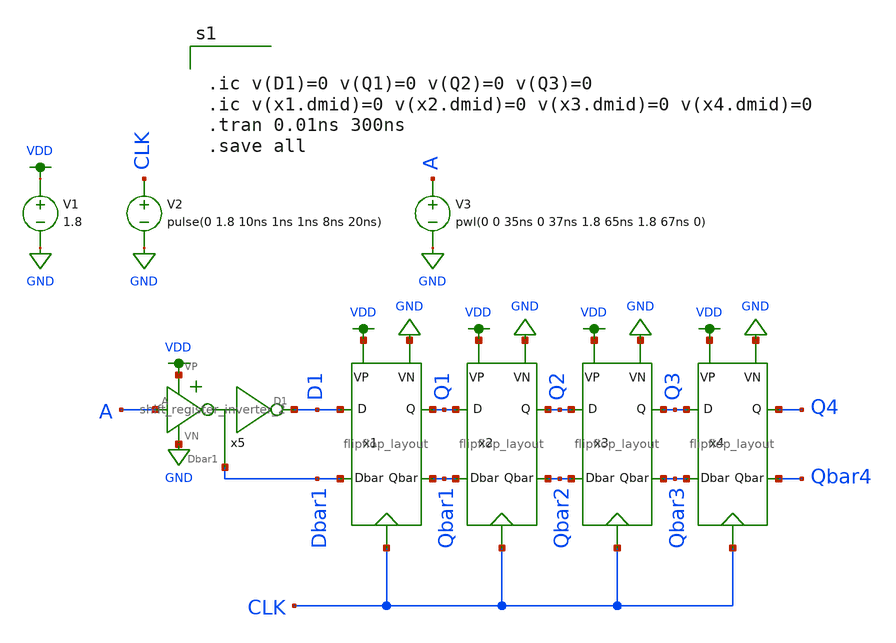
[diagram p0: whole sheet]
** sch_path: mp2/submission/Xschem/shift_register_test_sf.sch
**.subckt shift_register_test_sf
V1 VDD GND 1.8
V2 CLK GND pulse(0 1.8 10ns 1ns 1ns 8ns 20ns)
V3 A GND pwl(0 0 35ns 0 37ns 1.8 65ns 1.8 67ns 0)
x1 D1 VDD Dbar1 GND Q1 CLK Qbar1 flipflop_layout
x2 Q1 VDD Qbar1 GND Q2 CLK Qbar2 flipflop_layout
x3 Q2 VDD Qbar2 GND Q3 CLK Qbar3 flipflop_layout
x4 Q3 VDD Qbar3 GND Q4 CLK Qbar4 flipflop_layout
x5 VDD A D1 Dbar1 GND shift_register_inverter_2
**** begin user architecture code


.ic v(D1)=0 v(Q1)=0 v(Q2)=0 v(Q3)=0
.ic v(x1.dmid)=0 v(x2.dmid)=0 v(x3.dmid)=0 v(x4.dmid)=0
.tran 0.01ns 300ns
.save all


.option wnflag=1
.lib ~/skywater/skywater-pdk/libraries/sky130_fd_pr_ngspice/latest/models/sky130.lib.spice sf

**** end user architecture code
**.ends
.GLOBAL VDD
.GLOBAL GND
.end
